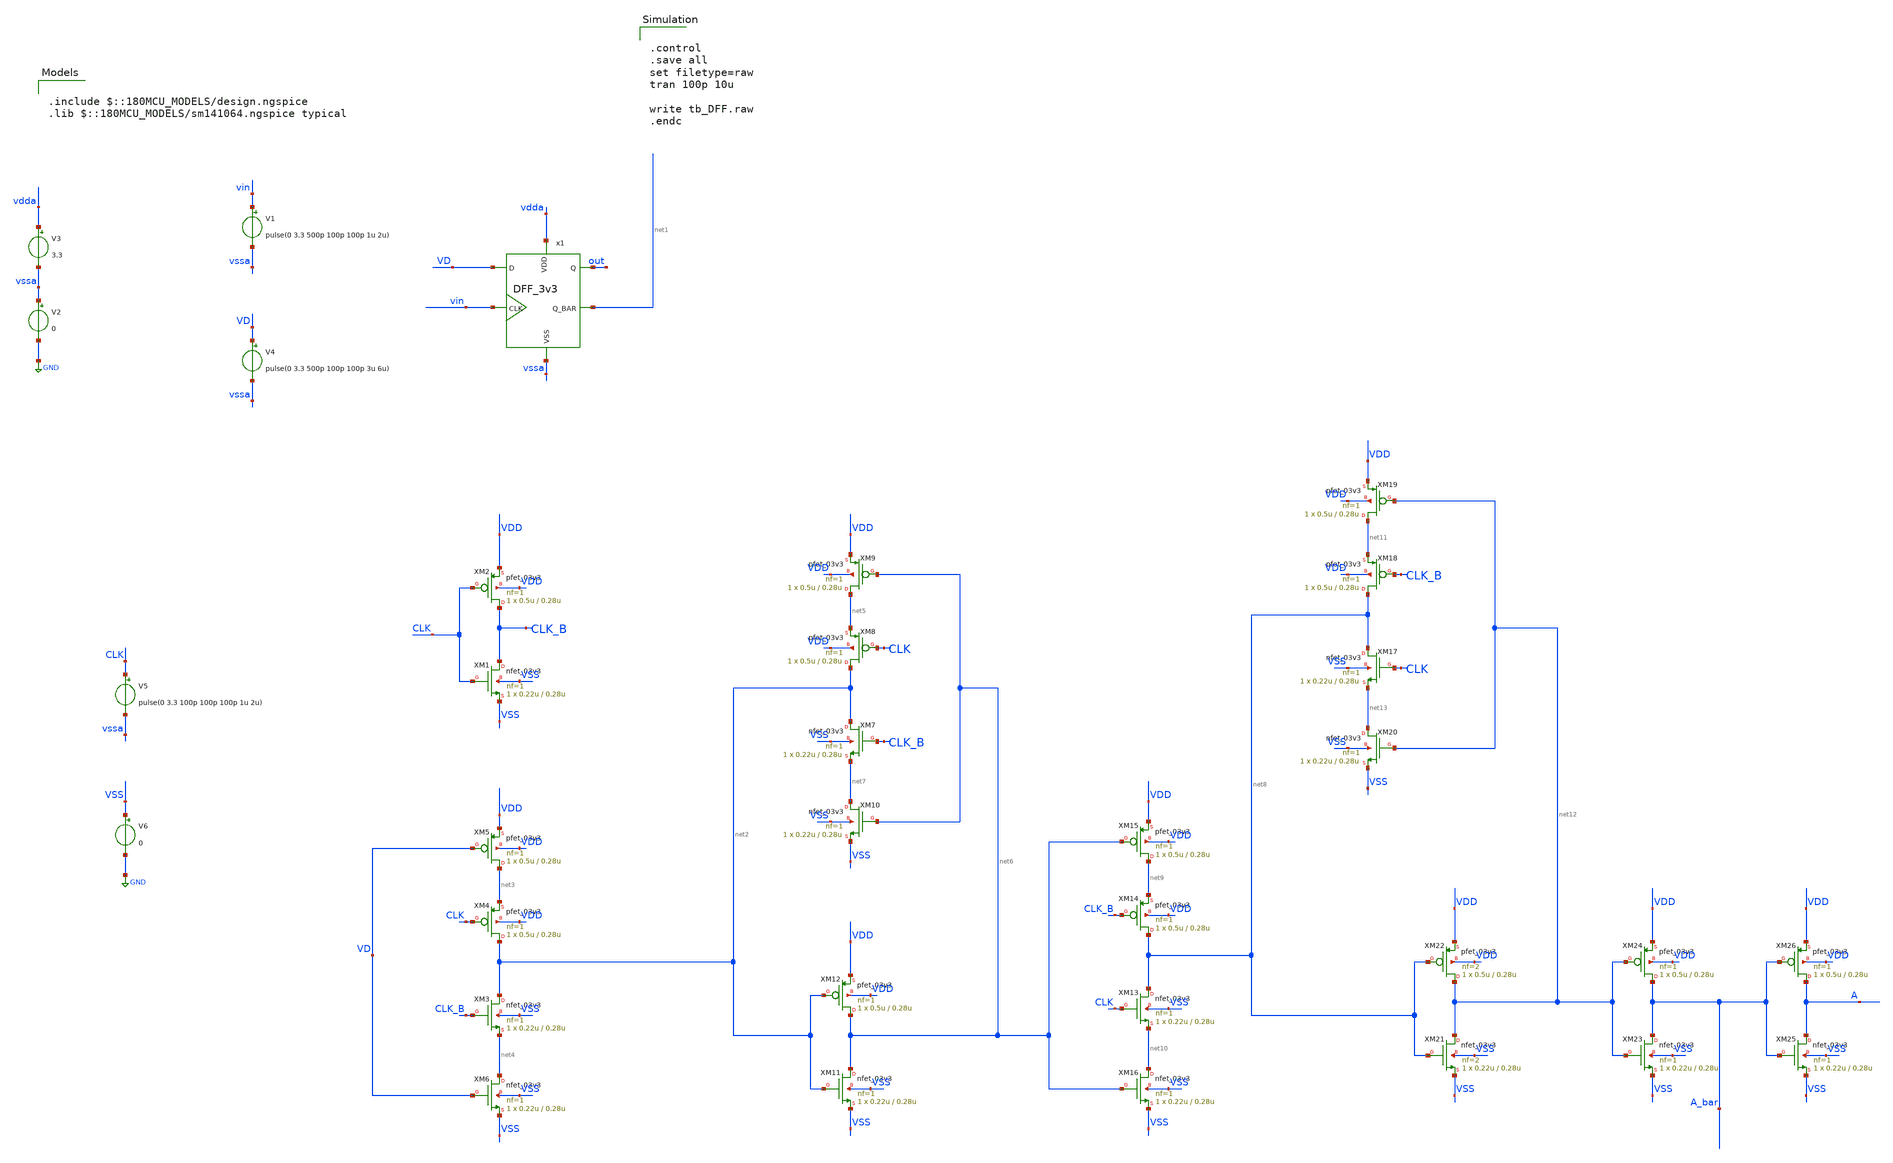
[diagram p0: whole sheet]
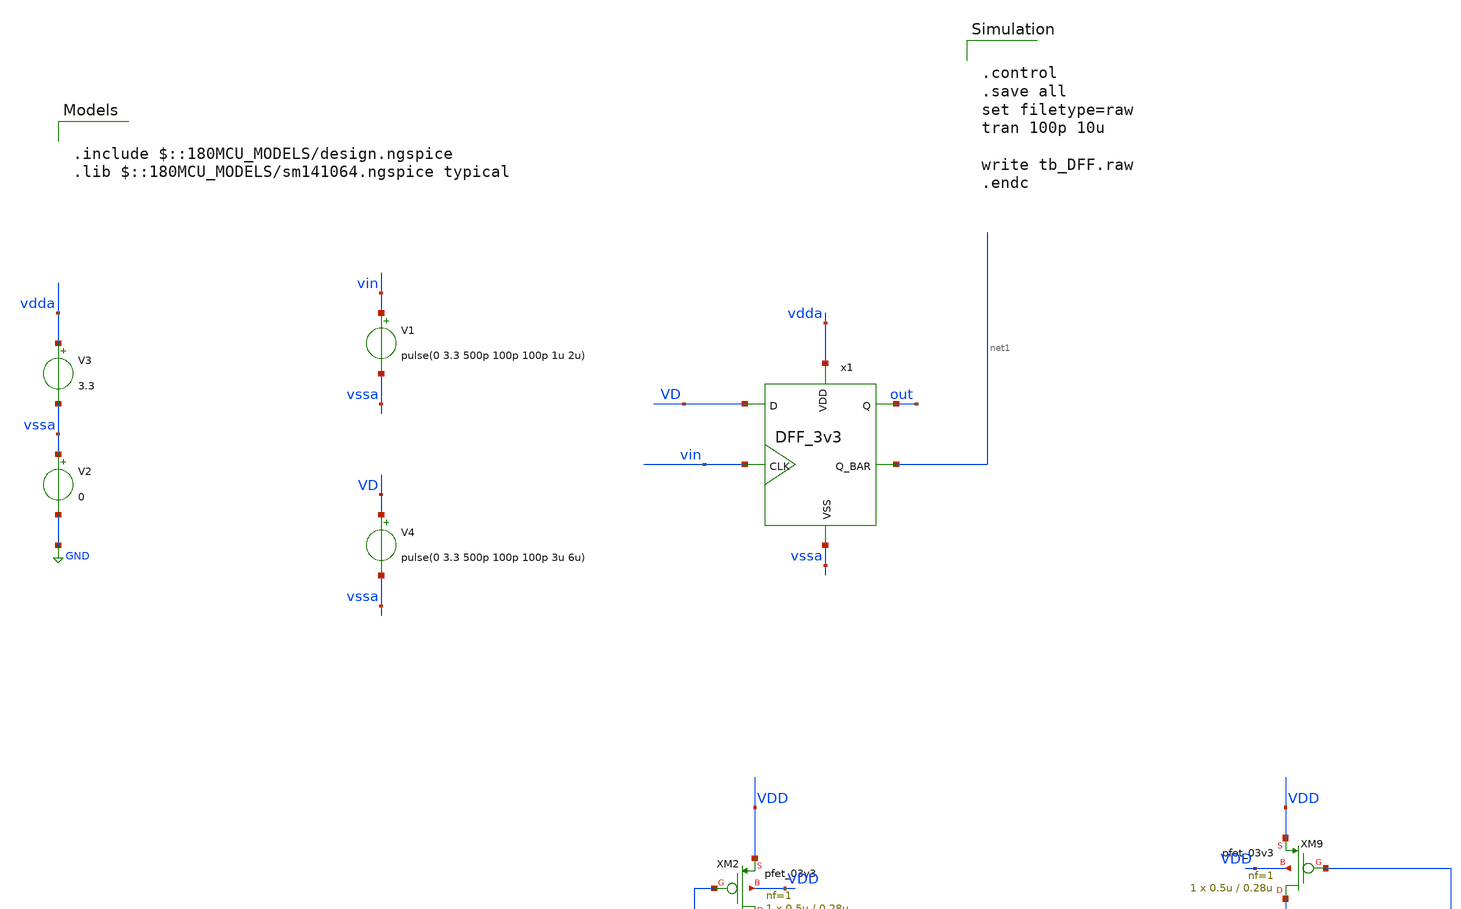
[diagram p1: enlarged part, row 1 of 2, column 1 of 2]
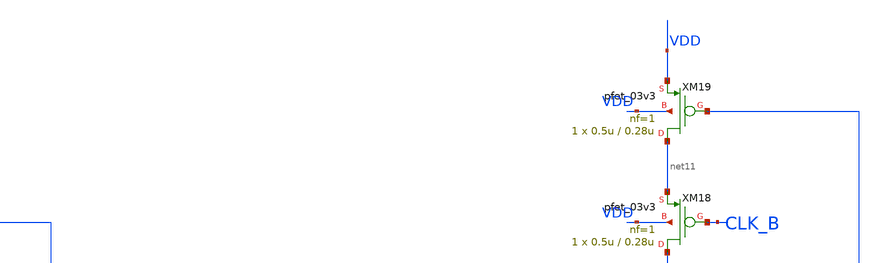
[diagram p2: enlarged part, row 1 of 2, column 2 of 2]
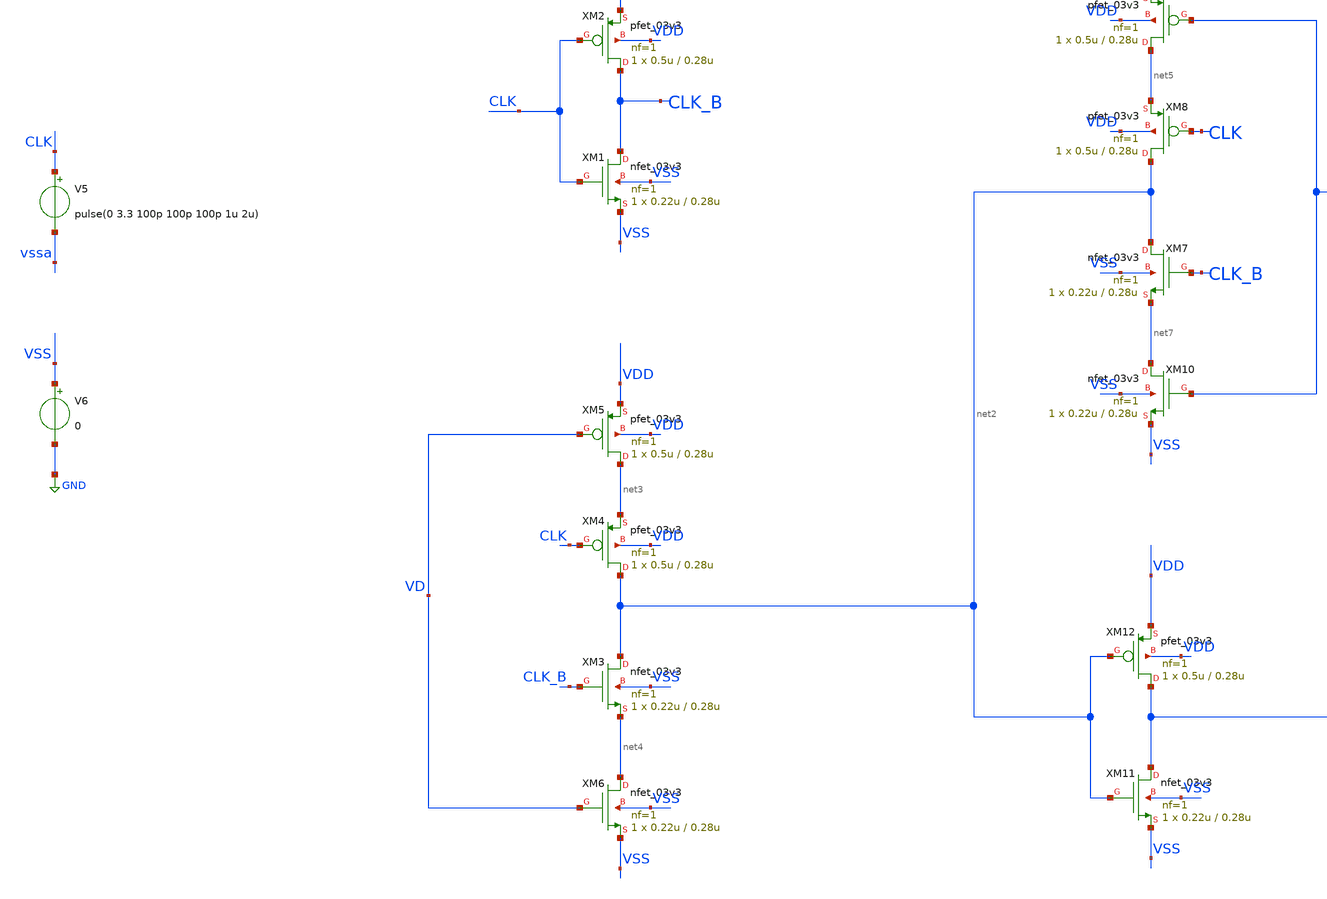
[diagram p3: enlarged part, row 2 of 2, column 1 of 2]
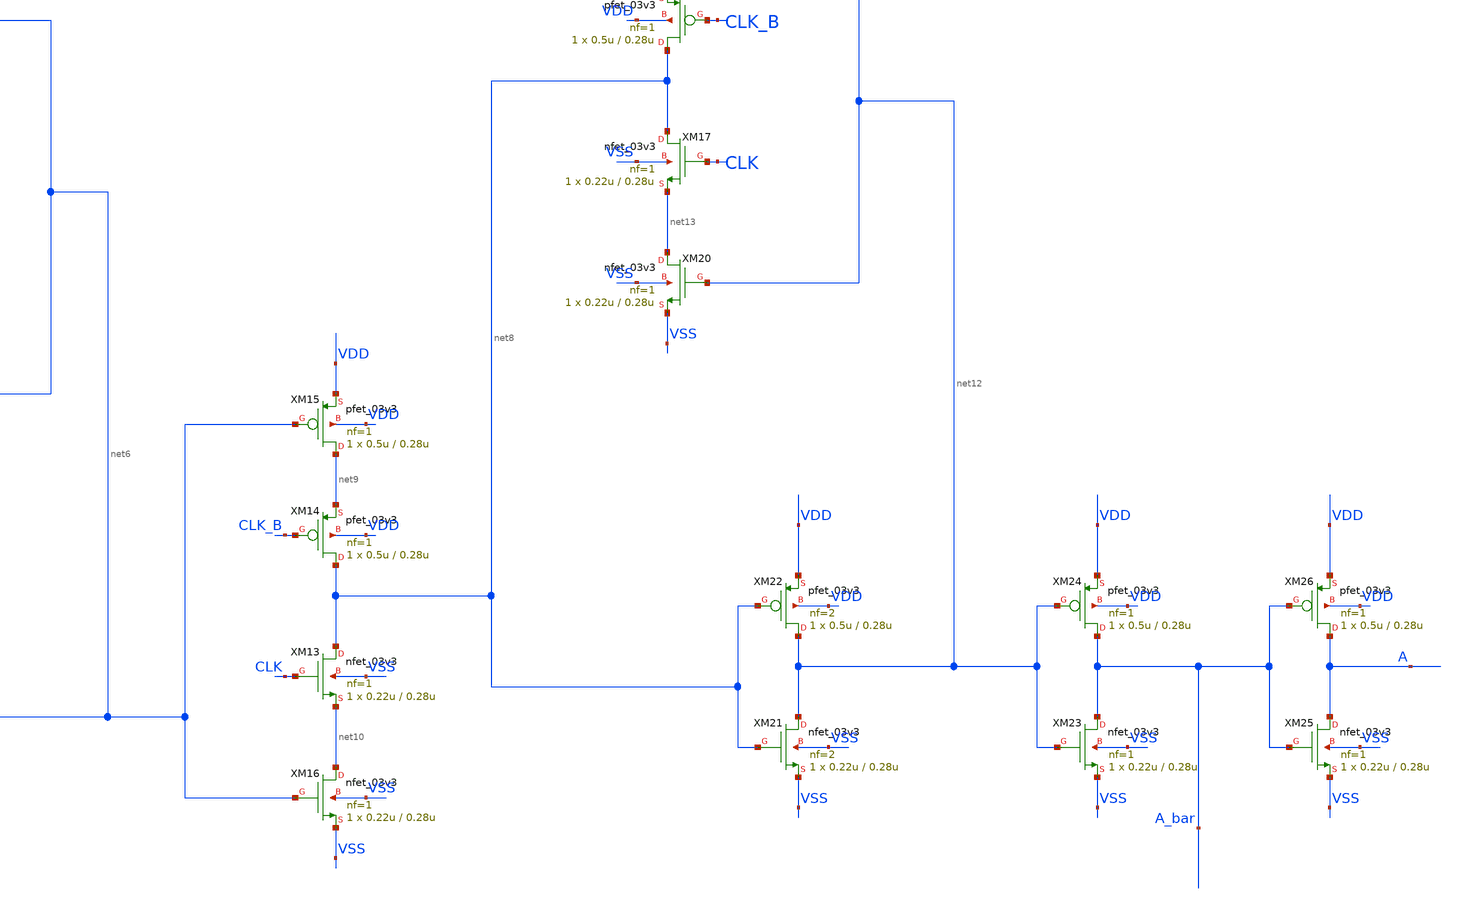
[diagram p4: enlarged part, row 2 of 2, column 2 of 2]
** sch_path: designs/DFF_TB.sch
**.subckt DFF_TB
V1 vin vssa pulse(0 3.3 500p 100p 100p 1u 2u)
V2 vssa GND 0
V3 vdda vssa 3.3
V4 VD vssa pulse(0 3.3 500p 100p 100p 3u 6u)
x1 vin vdda vssa VD out net1 DFF_3v3
XM1 CLK_B CLK VSS VSS nfet_03v3 L=0.28u W=0.22u nf=1 ad='int((nf+1)/2) * W/nf * 0.18u' as='int((nf+2)/2) * W/nf * 0.18u'
+ pd='2*int((nf+1)/2) * (W/nf + 0.18u)' ps='2*int((nf+2)/2) * (W/nf + 0.18u)' nrd='0.18u / W' nrs='0.18u / W'
+ sa=0 sb=0 sd=0 m=1
XM2 CLK_B CLK VDD VDD pfet_03v3 L=0.28u W=0.5u nf=1 ad='int((nf+1)/2) * W/nf * 0.18u' as='int((nf+2)/2) * W/nf * 0.18u'
+ pd='2*int((nf+1)/2) * (W/nf + 0.18u)' ps='2*int((nf+2)/2) * (W/nf + 0.18u)' nrd='0.18u / W' nrs='0.18u / W'
+ sa=0 sb=0 sd=0 m=1
XM3 net2 CLK_B net4 VSS nfet_03v3 L=0.28u W=0.22u nf=1 ad='int((nf+1)/2) * W/nf * 0.18u' as='int((nf+2)/2) * W/nf * 0.18u'
+ pd='2*int((nf+1)/2) * (W/nf + 0.18u)' ps='2*int((nf+2)/2) * (W/nf + 0.18u)' nrd='0.18u / W' nrs='0.18u / W'
+ sa=0 sb=0 sd=0 m=1
XM4 net2 CLK net3 VDD pfet_03v3 L=0.28u W=0.5u nf=1 ad='int((nf+1)/2) * W/nf * 0.18u' as='int((nf+2)/2) * W/nf * 0.18u'
+ pd='2*int((nf+1)/2) * (W/nf + 0.18u)' ps='2*int((nf+2)/2) * (W/nf + 0.18u)' nrd='0.18u / W' nrs='0.18u / W'
+ sa=0 sb=0 sd=0 m=1
XM5 net3 VD VDD VDD pfet_03v3 L=0.28u W=0.5u nf=1 ad='int((nf+1)/2) * W/nf * 0.18u' as='int((nf+2)/2) * W/nf * 0.18u'
+ pd='2*int((nf+1)/2) * (W/nf + 0.18u)' ps='2*int((nf+2)/2) * (W/nf + 0.18u)' nrd='0.18u / W' nrs='0.18u / W'
+ sa=0 sb=0 sd=0 m=1
XM6 net4 VD VSS VSS nfet_03v3 L=0.28u W=0.22u nf=1 ad='int((nf+1)/2) * W/nf * 0.18u' as='int((nf+2)/2) * W/nf * 0.18u'
+ pd='2*int((nf+1)/2) * (W/nf + 0.18u)' ps='2*int((nf+2)/2) * (W/nf + 0.18u)' nrd='0.18u / W' nrs='0.18u / W'
+ sa=0 sb=0 sd=0 m=1
XM7 net2 CLK_B net7 VSS nfet_03v3 L=0.28u W=0.22u nf=1 ad='int((nf+1)/2) * W/nf * 0.18u' as='int((nf+2)/2) * W/nf * 0.18u'
+ pd='2*int((nf+1)/2) * (W/nf + 0.18u)' ps='2*int((nf+2)/2) * (W/nf + 0.18u)' nrd='0.18u / W' nrs='0.18u / W'
+ sa=0 sb=0 sd=0 m=1
XM8 net2 CLK net5 VDD pfet_03v3 L=0.28u W=0.5u nf=1 ad='int((nf+1)/2) * W/nf * 0.18u' as='int((nf+2)/2) * W/nf * 0.18u'
+ pd='2*int((nf+1)/2) * (W/nf + 0.18u)' ps='2*int((nf+2)/2) * (W/nf + 0.18u)' nrd='0.18u / W' nrs='0.18u / W'
+ sa=0 sb=0 sd=0 m=1
XM9 net5 net6 VDD VDD pfet_03v3 L=0.28u W=0.5u nf=1 ad='int((nf+1)/2) * W/nf * 0.18u' as='int((nf+2)/2) * W/nf * 0.18u'
+ pd='2*int((nf+1)/2) * (W/nf + 0.18u)' ps='2*int((nf+2)/2) * (W/nf + 0.18u)' nrd='0.18u / W' nrs='0.18u / W'
+ sa=0 sb=0 sd=0 m=1
XM10 net7 net6 VSS VSS nfet_03v3 L=0.28u W=0.22u nf=1 ad='int((nf+1)/2) * W/nf * 0.18u' as='int((nf+2)/2) * W/nf * 0.18u'
+ pd='2*int((nf+1)/2) * (W/nf + 0.18u)' ps='2*int((nf+2)/2) * (W/nf + 0.18u)' nrd='0.18u / W' nrs='0.18u / W'
+ sa=0 sb=0 sd=0 m=1
XM11 net6 net2 VSS VSS nfet_03v3 L=0.28u W=0.22u nf=1 ad='int((nf+1)/2) * W/nf * 0.18u' as='int((nf+2)/2) * W/nf * 0.18u'
+ pd='2*int((nf+1)/2) * (W/nf + 0.18u)' ps='2*int((nf+2)/2) * (W/nf + 0.18u)' nrd='0.18u / W' nrs='0.18u / W'
+ sa=0 sb=0 sd=0 m=1
XM12 net6 net2 VDD VDD pfet_03v3 L=0.28u W=0.5u nf=1 ad='int((nf+1)/2) * W/nf * 0.18u' as='int((nf+2)/2) * W/nf * 0.18u'
+ pd='2*int((nf+1)/2) * (W/nf + 0.18u)' ps='2*int((nf+2)/2) * (W/nf + 0.18u)' nrd='0.18u / W' nrs='0.18u / W'
+ sa=0 sb=0 sd=0 m=1
XM13 net8 CLK net10 VSS nfet_03v3 L=0.28u W=0.22u nf=1 ad='int((nf+1)/2) * W/nf * 0.18u' as='int((nf+2)/2) * W/nf * 0.18u'
+ pd='2*int((nf+1)/2) * (W/nf + 0.18u)' ps='2*int((nf+2)/2) * (W/nf + 0.18u)' nrd='0.18u / W' nrs='0.18u / W'
+ sa=0 sb=0 sd=0 m=1
XM14 net8 CLK_B net9 VDD pfet_03v3 L=0.28u W=0.5u nf=1 ad='int((nf+1)/2) * W/nf * 0.18u' as='int((nf+2)/2) * W/nf * 0.18u'
+ pd='2*int((nf+1)/2) * (W/nf + 0.18u)' ps='2*int((nf+2)/2) * (W/nf + 0.18u)' nrd='0.18u / W' nrs='0.18u / W'
+ sa=0 sb=0 sd=0 m=1
XM15 net9 net6 VDD VDD pfet_03v3 L=0.28u W=0.5u nf=1 ad='int((nf+1)/2) * W/nf * 0.18u' as='int((nf+2)/2) * W/nf * 0.18u'
+ pd='2*int((nf+1)/2) * (W/nf + 0.18u)' ps='2*int((nf+2)/2) * (W/nf + 0.18u)' nrd='0.18u / W' nrs='0.18u / W'
+ sa=0 sb=0 sd=0 m=1
XM16 net10 net6 VSS VSS nfet_03v3 L=0.28u W=0.22u nf=1 ad='int((nf+1)/2) * W/nf * 0.18u' as='int((nf+2)/2) * W/nf * 0.18u'
+ pd='2*int((nf+1)/2) * (W/nf + 0.18u)' ps='2*int((nf+2)/2) * (W/nf + 0.18u)' nrd='0.18u / W' nrs='0.18u / W'
+ sa=0 sb=0 sd=0 m=1
XM17 net8 CLK net13 VSS nfet_03v3 L=0.28u W=0.22u nf=1 ad='int((nf+1)/2) * W/nf * 0.18u' as='int((nf+2)/2) * W/nf * 0.18u'
+ pd='2*int((nf+1)/2) * (W/nf + 0.18u)' ps='2*int((nf+2)/2) * (W/nf + 0.18u)' nrd='0.18u / W' nrs='0.18u / W'
+ sa=0 sb=0 sd=0 m=1
XM18 net8 CLK_B net11 VDD pfet_03v3 L=0.28u W=0.5u nf=1 ad='int((nf+1)/2) * W/nf * 0.18u' as='int((nf+2)/2) * W/nf * 0.18u'
+ pd='2*int((nf+1)/2) * (W/nf + 0.18u)' ps='2*int((nf+2)/2) * (W/nf + 0.18u)' nrd='0.18u / W' nrs='0.18u / W'
+ sa=0 sb=0 sd=0 m=1
XM19 net11 net12 VDD VDD pfet_03v3 L=0.28u W=0.5u nf=1 ad='int((nf+1)/2) * W/nf * 0.18u' as='int((nf+2)/2) * W/nf * 0.18u'
+ pd='2*int((nf+1)/2) * (W/nf + 0.18u)' ps='2*int((nf+2)/2) * (W/nf + 0.18u)' nrd='0.18u / W' nrs='0.18u / W'
+ sa=0 sb=0 sd=0 m=1
XM20 net13 net12 VSS VSS nfet_03v3 L=0.28u W=0.22u nf=1 ad='int((nf+1)/2) * W/nf * 0.18u' as='int((nf+2)/2) * W/nf * 0.18u'
+ pd='2*int((nf+1)/2) * (W/nf + 0.18u)' ps='2*int((nf+2)/2) * (W/nf + 0.18u)' nrd='0.18u / W' nrs='0.18u / W'
+ sa=0 sb=0 sd=0 m=1
XM21 net12 net8 VSS VSS nfet_03v3 L=0.28u W=0.22u nf=2 ad='int((nf+1)/2) * W/nf * 0.18u' as='int((nf+2)/2) * W/nf * 0.18u'
+ pd='2*int((nf+1)/2) * (W/nf + 0.18u)' ps='2*int((nf+2)/2) * (W/nf + 0.18u)' nrd='0.18u / W' nrs='0.18u / W'
+ sa=0 sb=0 sd=0 m=1
XM22 net12 net8 VDD VDD pfet_03v3 L=0.28u W=0.5u nf=2 ad='int((nf+1)/2) * W/nf * 0.18u' as='int((nf+2)/2) * W/nf * 0.18u'
+ pd='2*int((nf+1)/2) * (W/nf + 0.18u)' ps='2*int((nf+2)/2) * (W/nf + 0.18u)' nrd='0.18u / W' nrs='0.18u / W'
+ sa=0 sb=0 sd=0 m=1
XM23 A_bar net12 VSS VSS nfet_03v3 L=0.28u W=0.22u nf=1 ad='int((nf+1)/2) * W/nf * 0.18u' as='int((nf+2)/2) * W/nf * 0.18u'
+ pd='2*int((nf+1)/2) * (W/nf + 0.18u)' ps='2*int((nf+2)/2) * (W/nf + 0.18u)' nrd='0.18u / W' nrs='0.18u / W'
+ sa=0 sb=0 sd=0 m=1
XM24 A_bar net12 VDD VDD pfet_03v3 L=0.28u W=0.5u nf=1 ad='int((nf+1)/2) * W/nf * 0.18u' as='int((nf+2)/2) * W/nf * 0.18u'
+ pd='2*int((nf+1)/2) * (W/nf + 0.18u)' ps='2*int((nf+2)/2) * (W/nf + 0.18u)' nrd='0.18u / W' nrs='0.18u / W'
+ sa=0 sb=0 sd=0 m=1
XM25 A A_bar VSS VSS nfet_03v3 L=0.28u W=0.22u nf=1 ad='int((nf+1)/2) * W/nf * 0.18u' as='int((nf+2)/2) * W/nf * 0.18u'
+ pd='2*int((nf+1)/2) * (W/nf + 0.18u)' ps='2*int((nf+2)/2) * (W/nf + 0.18u)' nrd='0.18u / W' nrs='0.18u / W'
+ sa=0 sb=0 sd=0 m=1
XM26 A A_bar VDD VDD pfet_03v3 L=0.28u W=0.5u nf=1 ad='int((nf+1)/2) * W/nf * 0.18u' as='int((nf+2)/2) * W/nf * 0.18u'
+ pd='2*int((nf+1)/2) * (W/nf + 0.18u)' ps='2*int((nf+2)/2) * (W/nf + 0.18u)' nrd='0.18u / W' nrs='0.18u / W'
+ sa=0 sb=0 sd=0 m=1
V5 CLK vssa pulse(0 3.3 100p 100p 100p 1u 2u)
V6 VSS GND 0
**** begin user architecture code

.include $::180MCU_MODELS/design.ngspice
.lib $::180MCU_MODELS/sm141064.ngspice typical



.control
.save all
set filetype=raw
tran 100p 10u

write tb_DFF.raw
.endc


**** end user architecture code
**.ends

* expanding   symbol:  DFF_3v3.sym # of pins=6
** sym_path: designs/libs/qw_core_analog_pkedit/DFF_3v3.sym
** sch_path: designs/libs/qw_core_analog_pkedit/DFF_3v3.sch
.subckt DFF_3v3 CLK VDD VSS D Q Q_BAR
*.ipin CLK
*.ipin D
*.opin Q_BAR
*.ipin VDD
*.ipin VSS
*.opin Q
XM1 CLK_B CLK VSS VSS nfet_03v3 L=0.28u W=0.22u nf=1 ad='int((nf+1)/2) * W/nf * 0.18u' as='int((nf+2)/2) * W/nf * 0.18u'
+ pd='2*int((nf+1)/2) * (W/nf + 0.18u)' ps='2*int((nf+2)/2) * (W/nf + 0.18u)' nrd='0.18u / W' nrs='0.18u / W'
+ sa=0 sb=0 sd=0 m=1
XM2 CLK_B CLK VDD VDD pfet_03v3 L=0.28u W=0.5u nf=1 ad='int((nf+1)/2) * W/nf * 0.18u' as='int((nf+2)/2) * W/nf * 0.18u'
+ pd='2*int((nf+1)/2) * (W/nf + 0.18u)' ps='2*int((nf+2)/2) * (W/nf + 0.18u)' nrd='0.18u / W' nrs='0.18u / W'
+ sa=0 sb=0 sd=0 m=1
XM3 net1 CLK_B net3 VSS nfet_03v3 L=0.28u W=0.22u nf=1 ad='int((nf+1)/2) * W/nf * 0.18u' as='int((nf+2)/2) * W/nf * 0.18u'
+ pd='2*int((nf+1)/2) * (W/nf + 0.18u)' ps='2*int((nf+2)/2) * (W/nf + 0.18u)' nrd='0.18u / W' nrs='0.18u / W'
+ sa=0 sb=0 sd=0 m=1
XM4 net1 CLK net2 VDD pfet_03v3 L=0.28u W=0.5u nf=1 ad='int((nf+1)/2) * W/nf * 0.18u' as='int((nf+2)/2) * W/nf * 0.18u'
+ pd='2*int((nf+1)/2) * (W/nf + 0.18u)' ps='2*int((nf+2)/2) * (W/nf + 0.18u)' nrd='0.18u / W' nrs='0.18u / W'
+ sa=0 sb=0 sd=0 m=1
XM5 net2 D VDD VDD pfet_03v3 L=0.28u W=0.5u nf=1 ad='int((nf+1)/2) * W/nf * 0.18u' as='int((nf+2)/2) * W/nf * 0.18u'
+ pd='2*int((nf+1)/2) * (W/nf + 0.18u)' ps='2*int((nf+2)/2) * (W/nf + 0.18u)' nrd='0.18u / W' nrs='0.18u / W'
+ sa=0 sb=0 sd=0 m=1
XM6 net3 D VSS VSS nfet_03v3 L=0.28u W=0.22u nf=1 ad='int((nf+1)/2) * W/nf * 0.18u' as='int((nf+2)/2) * W/nf * 0.18u'
+ pd='2*int((nf+1)/2) * (W/nf + 0.18u)' ps='2*int((nf+2)/2) * (W/nf + 0.18u)' nrd='0.18u / W' nrs='0.18u / W'
+ sa=0 sb=0 sd=0 m=1
XM7 net1 CLK_B net6 VSS nfet_03v3 L=0.28u W=0.22u nf=1 ad='int((nf+1)/2) * W/nf * 0.18u' as='int((nf+2)/2) * W/nf * 0.18u'
+ pd='2*int((nf+1)/2) * (W/nf + 0.18u)' ps='2*int((nf+2)/2) * (W/nf + 0.18u)' nrd='0.18u / W' nrs='0.18u / W'
+ sa=0 sb=0 sd=0 m=1
XM8 net1 CLK net4 VDD pfet_03v3 L=0.28u W=0.5u nf=1 ad='int((nf+1)/2) * W/nf * 0.18u' as='int((nf+2)/2) * W/nf * 0.18u'
+ pd='2*int((nf+1)/2) * (W/nf + 0.18u)' ps='2*int((nf+2)/2) * (W/nf + 0.18u)' nrd='0.18u / W' nrs='0.18u / W'
+ sa=0 sb=0 sd=0 m=1
XM9 net4 net5 VDD VDD pfet_03v3 L=0.28u W=0.5u nf=1 ad='int((nf+1)/2) * W/nf * 0.18u' as='int((nf+2)/2) * W/nf * 0.18u'
+ pd='2*int((nf+1)/2) * (W/nf + 0.18u)' ps='2*int((nf+2)/2) * (W/nf + 0.18u)' nrd='0.18u / W' nrs='0.18u / W'
+ sa=0 sb=0 sd=0 m=1
XM10 net6 net5 VSS VSS nfet_03v3 L=0.28u W=0.22u nf=1 ad='int((nf+1)/2) * W/nf * 0.18u' as='int((nf+2)/2) * W/nf * 0.18u'
+ pd='2*int((nf+1)/2) * (W/nf + 0.18u)' ps='2*int((nf+2)/2) * (W/nf + 0.18u)' nrd='0.18u / W' nrs='0.18u / W'
+ sa=0 sb=0 sd=0 m=1
XM11 net5 net1 VSS VSS nfet_03v3 L=0.28u W=0.22u nf=1 ad='int((nf+1)/2) * W/nf * 0.18u' as='int((nf+2)/2) * W/nf * 0.18u'
+ pd='2*int((nf+1)/2) * (W/nf + 0.18u)' ps='2*int((nf+2)/2) * (W/nf + 0.18u)' nrd='0.18u / W' nrs='0.18u / W'
+ sa=0 sb=0 sd=0 m=1
XM12 net5 net1 VDD VDD pfet_03v3 L=0.28u W=0.5u nf=1 ad='int((nf+1)/2) * W/nf * 0.18u' as='int((nf+2)/2) * W/nf * 0.18u'
+ pd='2*int((nf+1)/2) * (W/nf + 0.18u)' ps='2*int((nf+2)/2) * (W/nf + 0.18u)' nrd='0.18u / W' nrs='0.18u / W'
+ sa=0 sb=0 sd=0 m=1
XM13 net7 CLK net9 VSS nfet_03v3 L=0.28u W=0.22u nf=1 ad='int((nf+1)/2) * W/nf * 0.18u' as='int((nf+2)/2) * W/nf * 0.18u'
+ pd='2*int((nf+1)/2) * (W/nf + 0.18u)' ps='2*int((nf+2)/2) * (W/nf + 0.18u)' nrd='0.18u / W' nrs='0.18u / W'
+ sa=0 sb=0 sd=0 m=1
XM14 net7 CLK_B net8 VDD pfet_03v3 L=0.28u W=0.5u nf=1 ad='int((nf+1)/2) * W/nf * 0.18u' as='int((nf+2)/2) * W/nf * 0.18u'
+ pd='2*int((nf+1)/2) * (W/nf + 0.18u)' ps='2*int((nf+2)/2) * (W/nf + 0.18u)' nrd='0.18u / W' nrs='0.18u / W'
+ sa=0 sb=0 sd=0 m=1
XM15 net8 net5 VDD VDD pfet_03v3 L=0.28u W=0.5u nf=1 ad='int((nf+1)/2) * W/nf * 0.18u' as='int((nf+2)/2) * W/nf * 0.18u'
+ pd='2*int((nf+1)/2) * (W/nf + 0.18u)' ps='2*int((nf+2)/2) * (W/nf + 0.18u)' nrd='0.18u / W' nrs='0.18u / W'
+ sa=0 sb=0 sd=0 m=1
XM16 net9 net5 VSS VSS nfet_03v3 L=0.28u W=0.22u nf=1 ad='int((nf+1)/2) * W/nf * 0.18u' as='int((nf+2)/2) * W/nf * 0.18u'
+ pd='2*int((nf+1)/2) * (W/nf + 0.18u)' ps='2*int((nf+2)/2) * (W/nf + 0.18u)' nrd='0.18u / W' nrs='0.18u / W'
+ sa=0 sb=0 sd=0 m=1
XM17 net7 CLK net12 VSS nfet_03v3 L=0.28u W=0.22u nf=1 ad='int((nf+1)/2) * W/nf * 0.18u' as='int((nf+2)/2) * W/nf * 0.18u'
+ pd='2*int((nf+1)/2) * (W/nf + 0.18u)' ps='2*int((nf+2)/2) * (W/nf + 0.18u)' nrd='0.18u / W' nrs='0.18u / W'
+ sa=0 sb=0 sd=0 m=1
XM18 net7 CLK_B net10 VDD pfet_03v3 L=0.28u W=0.5u nf=1 ad='int((nf+1)/2) * W/nf * 0.18u' as='int((nf+2)/2) * W/nf * 0.18u'
+ pd='2*int((nf+1)/2) * (W/nf + 0.18u)' ps='2*int((nf+2)/2) * (W/nf + 0.18u)' nrd='0.18u / W' nrs='0.18u / W'
+ sa=0 sb=0 sd=0 m=1
XM19 net10 net11 VDD VDD pfet_03v3 L=0.28u W=0.5u nf=1 ad='int((nf+1)/2) * W/nf * 0.18u' as='int((nf+2)/2) * W/nf * 0.18u'
+ pd='2*int((nf+1)/2) * (W/nf + 0.18u)' ps='2*int((nf+2)/2) * (W/nf + 0.18u)' nrd='0.18u / W' nrs='0.18u / W'
+ sa=0 sb=0 sd=0 m=1
XM20 net12 net11 VSS VSS nfet_03v3 L=0.28u W=0.22u nf=1 ad='int((nf+1)/2) * W/nf * 0.18u' as='int((nf+2)/2) * W/nf * 0.18u'
+ pd='2*int((nf+1)/2) * (W/nf + 0.18u)' ps='2*int((nf+2)/2) * (W/nf + 0.18u)' nrd='0.18u / W' nrs='0.18u / W'
+ sa=0 sb=0 sd=0 m=1
XM21 net11 net7 VSS VSS nfet_03v3 L=0.28u W=0.22u nf=2 ad='int((nf+1)/2) * W/nf * 0.18u' as='int((nf+2)/2) * W/nf * 0.18u'
+ pd='2*int((nf+1)/2) * (W/nf + 0.18u)' ps='2*int((nf+2)/2) * (W/nf + 0.18u)' nrd='0.18u / W' nrs='0.18u / W'
+ sa=0 sb=0 sd=0 m=1
XM22 net11 net7 VDD VDD pfet_03v3 L=0.28u W=0.5u nf=2 ad='int((nf+1)/2) * W/nf * 0.18u' as='int((nf+2)/2) * W/nf * 0.18u'
+ pd='2*int((nf+1)/2) * (W/nf + 0.18u)' ps='2*int((nf+2)/2) * (W/nf + 0.18u)' nrd='0.18u / W' nrs='0.18u / W'
+ sa=0 sb=0 sd=0 m=1
XM23 Q_BAR net11 VSS VSS nfet_03v3 L=0.28u W=0.22u nf=1 ad='int((nf+1)/2) * W/nf * 0.18u' as='int((nf+2)/2) * W/nf * 0.18u'
+ pd='2*int((nf+1)/2) * (W/nf + 0.18u)' ps='2*int((nf+2)/2) * (W/nf + 0.18u)' nrd='0.18u / W' nrs='0.18u / W'
+ sa=0 sb=0 sd=0 m=1
XM24 Q_BAR net11 VDD VDD pfet_03v3 L=0.28u W=0.5u nf=1 ad='int((nf+1)/2) * W/nf * 0.18u' as='int((nf+2)/2) * W/nf * 0.18u'
+ pd='2*int((nf+1)/2) * (W/nf + 0.18u)' ps='2*int((nf+2)/2) * (W/nf + 0.18u)' nrd='0.18u / W' nrs='0.18u / W'
+ sa=0 sb=0 sd=0 m=1
XM25 Q Q_BAR VSS VSS nfet_03v3 L=0.28u W=0.22u nf=1 ad='int((nf+1)/2) * W/nf * 0.18u' as='int((nf+2)/2) * W/nf * 0.18u'
+ pd='2*int((nf+1)/2) * (W/nf + 0.18u)' ps='2*int((nf+2)/2) * (W/nf + 0.18u)' nrd='0.18u / W' nrs='0.18u / W'
+ sa=0 sb=0 sd=0 m=1
XM26 Q Q_BAR VDD VDD pfet_03v3 L=0.28u W=0.5u nf=1 ad='int((nf+1)/2) * W/nf * 0.18u' as='int((nf+2)/2) * W/nf * 0.18u'
+ pd='2*int((nf+1)/2) * (W/nf + 0.18u)' ps='2*int((nf+2)/2) * (W/nf + 0.18u)' nrd='0.18u / W' nrs='0.18u / W'
+ sa=0 sb=0 sd=0 m=1
.ends

.GLOBAL GND
.end
